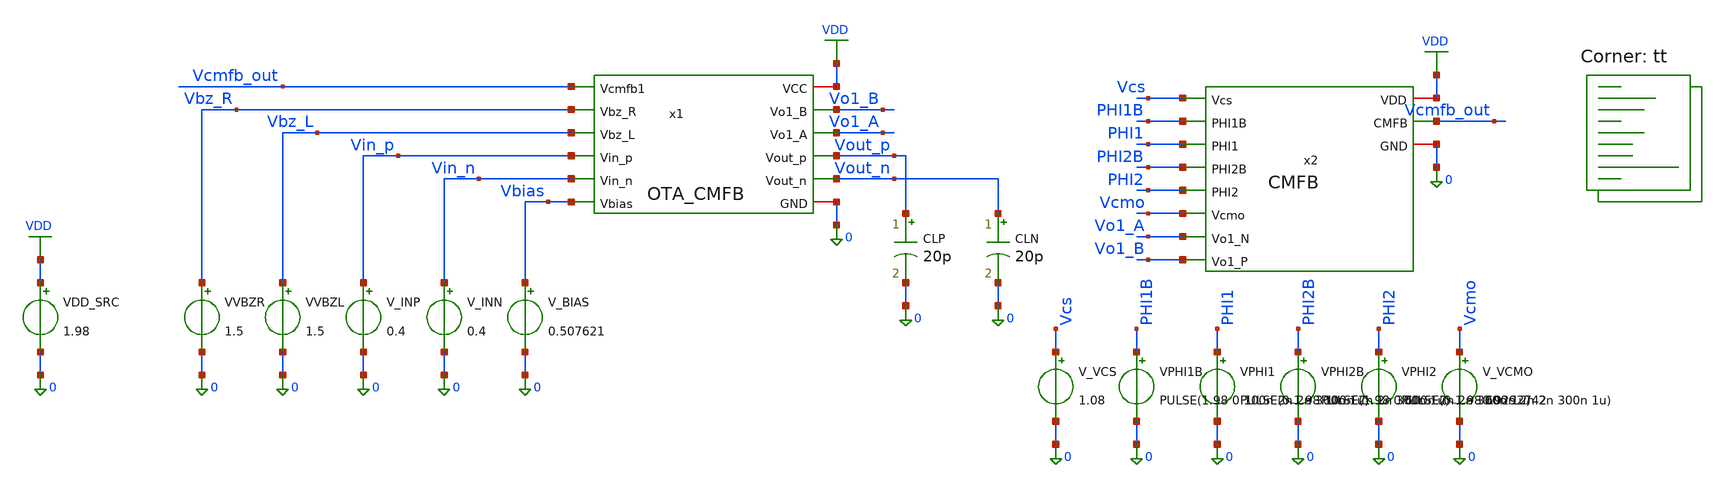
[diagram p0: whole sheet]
** sch_path: blocks/02_CMFB/sim/tb_OTA_CMFB_Vcs_sweep_TT_1v98_27C.sch
**.subckt tb_OTA_CMFB_Vcs_sweep_TT_1v98_27C
x1 VDD Vcmfb_out Vbz_R Vbz_L Vin_p Vin_n Vo1_B Vo1_A Vout_p Vout_n Vbias 0 OTA_CMFB
x2 Vcmfb_out Vcs PHI1B PHI1 VDD PHI2B 0 PHI2 Vcmo Vo1_A Vo1_B CMFB
VDD_SRC VDD 0 1.98
VVBZR Vbz_R 0 1.5
VVBZL Vbz_L 0 1.5
V_INP Vin_p 0 0.4
V_INN Vin_n 0 0.4
V_BIAS Vbias 0 0.507621
CLP Vout_p 0 20p m=1
CLN Vout_n 0 20p m=1
V_VCS Vcs 0 1.08
VPHI1B PHI1B 0 PULSE(1.98 0 100n 2n 2n 300n 1u)
VPHI1 PHI1 0 PULSE(0 1.98 100n 2n 2n 300n 1u)
VPHI2B PHI2B 0 PULSE(1.98 0 600n 2n 2n 300n 1u)
VPHI2 PHI2 0 PULSE(0 1.98 600n 2n 2n 300n 1u)
V_VCMO Vcmo 0 0.9292742
**** begin user architecture code
.lib $::SKYWATER_MODELS/sky130.lib.spice tt


* ============================================================
* OTA + SC-CMFB | FIRST-STAGE VCS BIAS CHARACTERIZATION
* TT, 27 C, VDD = 1.98 V
* VCS test points: 0.70 0.80 0.85 0.90 0.95 1.00 1.10
*
* Closed-loop schematic is unchanged, except VDD and clock high
* (clock high follows VDD for this fixed-bias screening).
* Vbias = 0.507621, Vbz L/R = 1.5, Vcmo = 0.9292742 V.
* Each test point starts with RESET and an independent transient.
* This is a DIAGNOSTIC scan, not an optimized bias network.
* ============================================================
.temp 27
.options rshunt=1e12
RLEAK_CMFB Vcmfb_out 0 1e12
.control
save all

echo =========================================================
echo VCS BIAS CHARACTERIZATION | TT | VDD 1.98 | TEMP 27 C
echo =========================================================

foreach vcsval 0.70 0.80 0.85 0.90 0.95 1.00 1.10
  reset
  alter V_VCS $vcsval
  save all
  echo ---------------------------------------------------------
  echo VDD 1.98 V | VCS $vcsval V | START
  tran 1n 100u

  let vo1cm = (v(vo1_a)+v(vo1_b))/2
  let vocm = (v(vout_p)+v(vout_n))/2
  let vo1d = v(vo1_a)-v(vo1_b)
  let vod = v(vout_p)-v(vout_n)

  meas tran VO1CM_AVG AVG vo1cm FROM=90u TO=100u
  meas tran VO1CM_PREV AVG vo1cm FROM=80u TO=90u
  meas tran VO1CM_MIN MIN vo1cm FROM=90u TO=100u
  meas tran VO1CM_MAX MAX vo1cm FROM=90u TO=100u

  meas tran VCMFB_AVG AVG v(vcmfb_out) FROM=90u TO=100u
  meas tran VCMFB_PREV AVG v(vcmfb_out) FROM=80u TO=90u
  meas tran VCMFB_MIN MIN v(vcmfb_out) FROM=90u TO=100u
  meas tran VCMFB_MAX MAX v(vcmfb_out) FROM=90u TO=100u

  meas tran VOUTCM_AVG AVG vocm FROM=90u TO=100u
  meas tran VOUTCM_PREV AVG vocm FROM=80u TO=90u
  meas tran VOUTCM_MIN MIN vocm FROM=90u TO=100u
  meas tran VOUTCM_MAX MAX vocm FROM=90u TO=100u
  meas tran VOD_AVG AVG vod FROM=90u TO=100u
  meas tran VO1D_AVG AVG vo1d FROM=90u TO=100u

  let VCS_APPLIED = $vcsval
  let VO1CM_ERROR = VO1CM_AVG - 0.9292742
  let VO1CM_RIPPLE = VO1CM_MAX - VO1CM_MIN
  let CTRL_RIPPLE = VCMFB_MAX - VCMFB_MIN
  let VOUTCM_RIPPLE = VOUTCM_MAX - VOUTCM_MIN
  let VO1CM_DRIFT = VO1CM_AVG - VO1CM_PREV
  let CTRL_DRIFT = VCMFB_AVG - VCMFB_PREV
  let VOUTCM_DRIFT = VOUTCM_AVG - VOUTCM_PREV

  echo ========= BEGIN BIAS SWEEP RESULT =========
  echo VDD 1.98 V | VCS $vcsval V | TT | 27 C
  print VCS_APPLIED VO1CM_AVG VO1CM_ERROR VO1CM_RIPPLE
  print VCMFB_AVG CTRL_RIPPLE
  print VOUTCM_AVG VOUTCM_RIPPLE VOD_AVG VO1D_AVG
  print VO1CM_DRIFT CTRL_DRIFT VOUTCM_DRIFT
  echo ========= END BIAS SWEEP RESULT =========
end

echo ALL VCS POINTS COMPLETED FOR VDD 1.98 V
.endc


**** end user architecture code
**.ends
.GLOBAL VDD
.end
